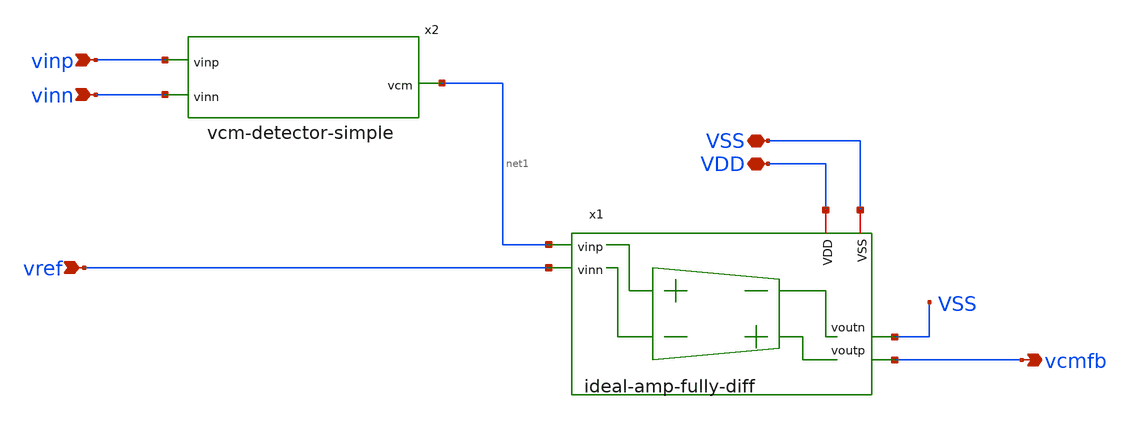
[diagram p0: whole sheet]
** sch_path: analog-db/drawings/shared/ideal/cmfb-output-ideal-amp.sch
* Copyright 2026 MacAnalog Research Group
**.subckt cmfb-output-ideal-amp VSS VDD vinp vinn vcmfb vref
*.iopin VSS
*.iopin VDD
*.ipin vinp
*.ipin vinn
*.opin vcmfb
*.ipin vref
x1 net1 vref VSS vcmfb VSS VDD ideal-amp-fully-diff
x2 net1 vinp vinn vcm-detector-simple
**.ends
.end
